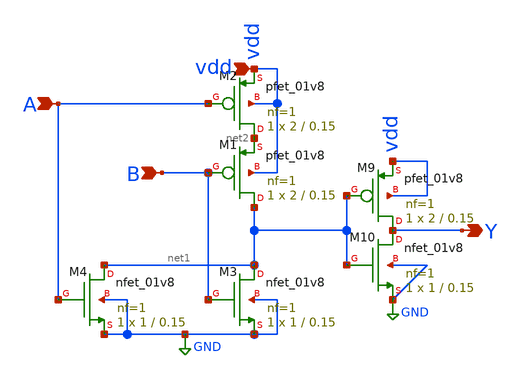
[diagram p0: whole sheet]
** sch_path: Circuit Files/Logic gate design using MOSFETS/gates/OR_gate.sch
**.subckt OR_gate A B vdd Y
*.ipin A
*.ipin B
*.ipin vdd
*.opin Y
XM1 net1 B net2 vdd sky130_fd_pr__pfet_01v8 L=0.15 W=2 nf=1 ad='int((nf+1)/2) * W/nf * 0.29' as='int((nf+2)/2) * W/nf * 0.29'
+ pd='2*int((nf+1)/2) * (W/nf + 0.29)' ps='2*int((nf+2)/2) * (W/nf + 0.29)' nrd='0.29 / W' nrs='0.29 / W'
+ sa=0 sb=0 sd=0 mult=1 m=1
XM2 net2 A vdd vdd sky130_fd_pr__pfet_01v8 L=0.15 W=2 nf=1 ad='int((nf+1)/2) * W/nf * 0.29' as='int((nf+2)/2) * W/nf * 0.29'
+ pd='2*int((nf+1)/2) * (W/nf + 0.29)' ps='2*int((nf+2)/2) * (W/nf + 0.29)' nrd='0.29 / W' nrs='0.29 / W'
+ sa=0 sb=0 sd=0 mult=1 m=1
XM3 net1 B GND GND sky130_fd_pr__nfet_01v8 L=0.15 W=1 nf=1 ad='int((nf+1)/2) * W/nf * 0.29' as='int((nf+2)/2) * W/nf * 0.29'
+ pd='2*int((nf+1)/2) * (W/nf + 0.29)' ps='2*int((nf+2)/2) * (W/nf + 0.29)' nrd='0.29 / W' nrs='0.29 / W'
+ sa=0 sb=0 sd=0 mult=1 m=1
XM4 net1 A GND GND sky130_fd_pr__nfet_01v8 L=0.15 W=1 nf=1 ad='int((nf+1)/2) * W/nf * 0.29' as='int((nf+2)/2) * W/nf * 0.29'
+ pd='2*int((nf+1)/2) * (W/nf + 0.29)' ps='2*int((nf+2)/2) * (W/nf + 0.29)' nrd='0.29 / W' nrs='0.29 / W'
+ sa=0 sb=0 sd=0 mult=1 m=1
XM9 Y net1 vdd vdd sky130_fd_pr__pfet_01v8 L=0.15 W=2 nf=1 ad='int((nf+1)/2) * W/nf * 0.29' as='int((nf+2)/2) * W/nf * 0.29'
+ pd='2*int((nf+1)/2) * (W/nf + 0.29)' ps='2*int((nf+2)/2) * (W/nf + 0.29)' nrd='0.29 / W' nrs='0.29 / W'
+ sa=0 sb=0 sd=0 mult=1 m=1
XM10 Y net1 GND GND sky130_fd_pr__nfet_01v8 L=0.15 W=1 nf=1 ad='int((nf+1)/2) * W/nf * 0.29' as='int((nf+2)/2) * W/nf * 0.29'
+ pd='2*int((nf+1)/2) * (W/nf + 0.29)' ps='2*int((nf+2)/2) * (W/nf + 0.29)' nrd='0.29 / W' nrs='0.29 / W'
+ sa=0 sb=0 sd=0 mult=1 m=1
**.ends
.GLOBAL GND
.end
